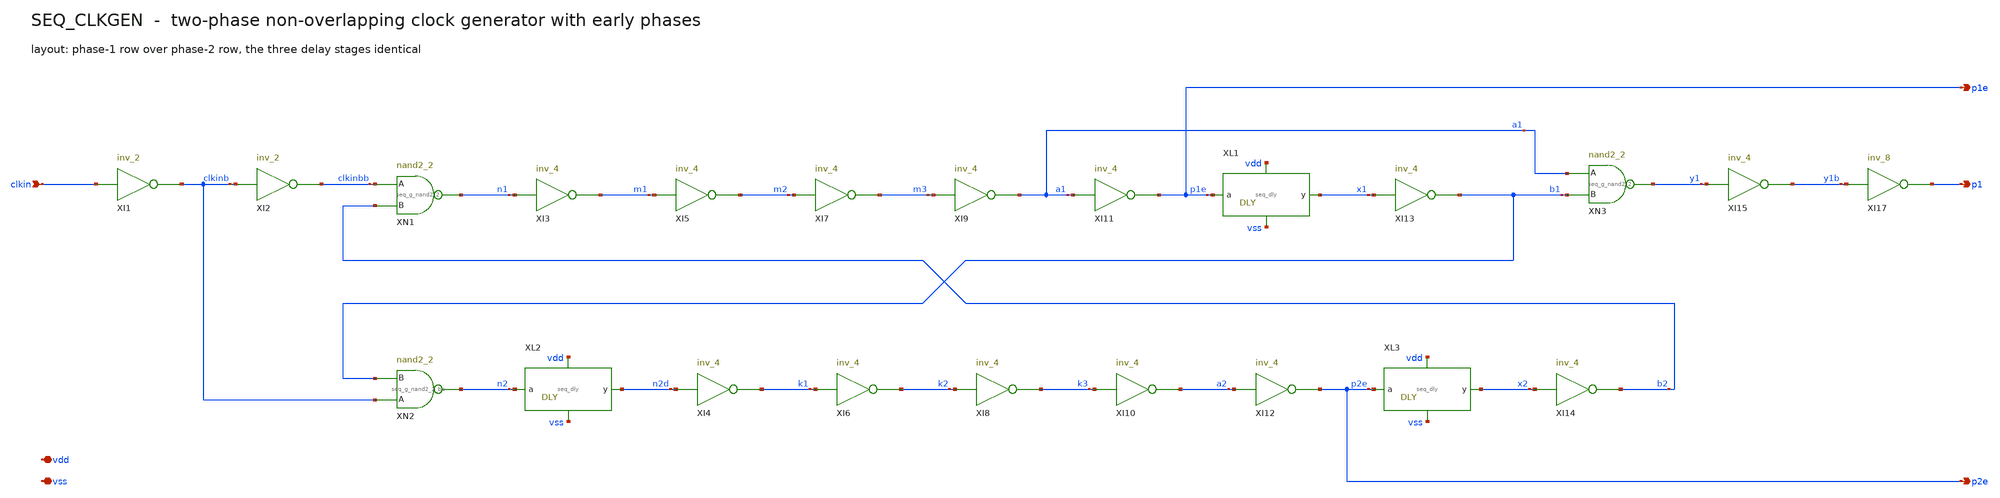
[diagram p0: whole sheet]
** sch_path: mixed_signal/sample_seq/seq_clkgen.sch
**.subckt seq_clkgen clkin p1e p1 p2e vdd vss
*.ipin clkin
*.opin p1e
*.opin p1
*.opin p2e
*.iopin vdd
*.iopin vss
XI1 vdd vdd vss vss clkinb clkin gf180mcu_as_sc_mcu7t3v3__inv_2
XI2 vdd vdd vss vss clkinbb clkinb gf180mcu_as_sc_mcu7t3v3__inv_2
XN1 vdd vdd vss vss n1 b2 clkinbb gf180mcu_as_sc_mcu7t3v3__nand2_2
XI3 vdd vdd vss vss m1 n1 gf180mcu_as_sc_mcu7t3v3__inv_4
XI5 vdd vdd vss vss m2 m1 gf180mcu_as_sc_mcu7t3v3__inv_4
XI7 vdd vdd vss vss m3 m2 gf180mcu_as_sc_mcu7t3v3__inv_4
XI9 vdd vdd vss vss a1 m3 gf180mcu_as_sc_mcu7t3v3__inv_4
XI11 vdd vdd vss vss p1e a1 gf180mcu_as_sc_mcu7t3v3__inv_4
XL1 p1e x1 vdd vss seq_dly
XI13 vdd vdd vss vss b1 x1 gf180mcu_as_sc_mcu7t3v3__inv_4
XN3 vdd vdd vss vss y1 b1 a1 gf180mcu_as_sc_mcu7t3v3__nand2_2
XI15 vdd vdd vss vss y1b y1 gf180mcu_as_sc_mcu7t3v3__inv_4
XI17 vdd vdd vss vss p1 y1b gf180mcu_as_sc_mcu7t3v3__inv_8
XN2 vdd vdd vss vss n2 b1 clkinb gf180mcu_as_sc_mcu7t3v3__nand2_2
XL2 n2 n2d vdd vss seq_dly
XI4 vdd vdd vss vss k1 n2d gf180mcu_as_sc_mcu7t3v3__inv_4
XI6 vdd vdd vss vss k2 k1 gf180mcu_as_sc_mcu7t3v3__inv_4
XI8 vdd vdd vss vss k3 k2 gf180mcu_as_sc_mcu7t3v3__inv_4
XI10 vdd vdd vss vss a2 k3 gf180mcu_as_sc_mcu7t3v3__inv_4
XI12 vdd vdd vss vss p2e a2 gf180mcu_as_sc_mcu7t3v3__inv_4
XL3 p2e x2 vdd vss seq_dly
XI14 vdd vdd vss vss b2 x2 gf180mcu_as_sc_mcu7t3v3__inv_4
**.ends

* expanding   symbol:  seq_dly.sym # of pins=4
** sym_path: mixed_signal/sample_seq/seq_dly.sym
** sch_path: mixed_signal/sample_seq/seq_dly.sch
.subckt seq_dly a y vdd vss
*.ipin a
*.opin y
*.iopin vdd
*.iopin vss
XD1 vdd vdd vss vss d1 a gf180mcu_as_sc_mcu7t3v3__inv_2
XD2 vdd vdd vss vss d2 d1 gf180mcu_as_sc_mcu7t3v3__inv_2
XD3 vdd vdd vss vss d3 d2 gf180mcu_as_sc_mcu7t3v3__inv_2
XD4 vdd vdd vss vss y d3 gf180mcu_as_sc_mcu7t3v3__inv_2
.ends

.end
